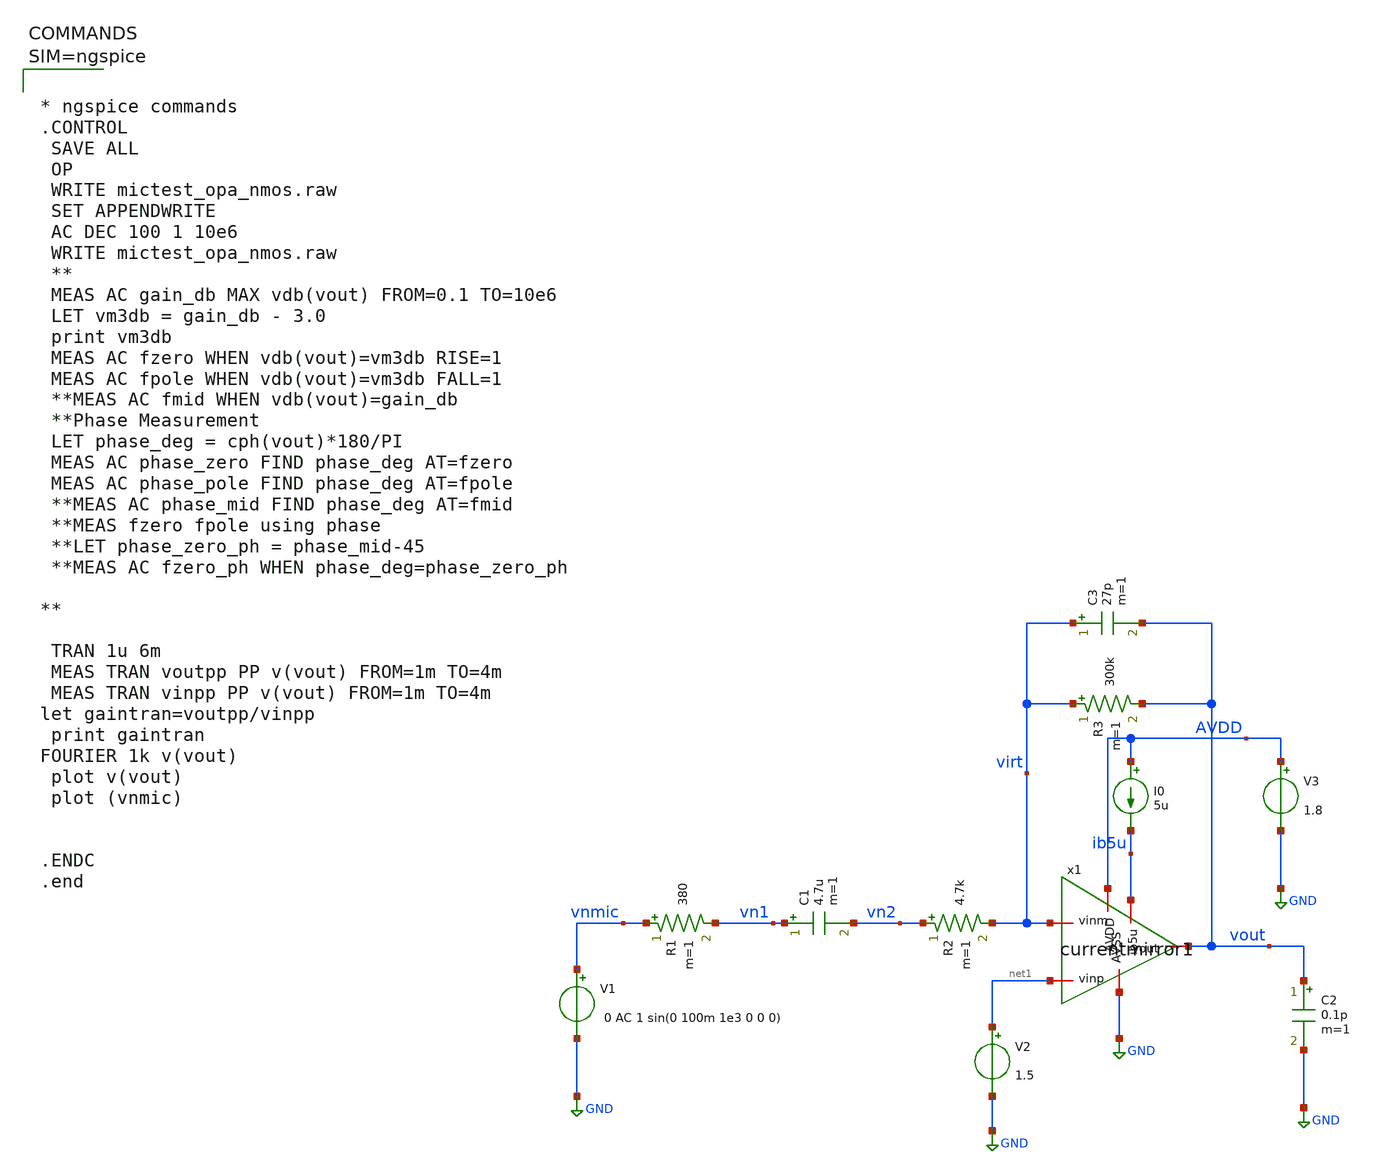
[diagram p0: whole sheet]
** sch_path: xschem/mictest_opamp_nmos.sch
**.subckt mictest_opamp_nmos
x1 AVDD vout virt net1 ib5u GND currentmirror1
R1 vnmic vn1 380 m=1
R2 vn2 virt 4.7k m=1
C1 vn1 vn2 4.7u m=1
V1 vnmic GND 0 AC 1 sin(0 100m 1e3 0 0 0)
I0 AVDD ib5u 5u
V2 net1 GND 1.5
C2 vout GND 0.1p m=1
V3 AVDD GND 1.8
R3 virt vout 300k m=1
C3 virt vout 27p m=1
**** begin user architecture code

** opencircuitdesign pdks install
.lib $::SKYWATER_MODELS/sky130.lib.spice tt




* ngspice commands
.CONTROL
 SAVE ALL
 OP
 WRITE mictest_opa_nmos.raw
 SET APPENDWRITE
 AC DEC 100 1 10e6
 WRITE mictest_opa_nmos.raw
 **
 MEAS AC gain_db MAX vdb(vout) FROM=0.1 TO=10e6
 LET vm3db = gain_db - 3.0
 print vm3db
 MEAS AC fzero WHEN vdb(vout)=vm3db RISE=1
 MEAS AC fpole WHEN vdb(vout)=vm3db FALL=1
 **MEAS AC fmid WHEN vdb(vout)=gain_db
 **Phase Measurement
 LET phase_deg = cph(vout)*180/PI
 MEAS AC phase_zero FIND phase_deg AT=fzero
 MEAS AC phase_pole FIND phase_deg AT=fpole
 **MEAS AC phase_mid FIND phase_deg AT=fmid
 **MEAS fzero fpole using phase
 **LET phase_zero_ph = phase_mid-45
 **MEAS AC fzero_ph WHEN phase_deg=phase_zero_ph

**

 TRAN 1u 6m
 MEAS TRAN voutpp PP v(vout) FROM=1m TO=4m
 MEAS TRAN vinpp PP v(vout) FROM=1m TO=4m
let gaintran=voutpp/vinpp
 print gaintran
FOURIER 1k v(vout)
 plot v(vout)
 plot (vnmic)


.ENDC
.end



**** end user architecture code
**.ends

* expanding   symbol:  currentmirror1.sym # of pins=6
** sym_path: xschem/currentmirror1.sym
** sch_path: xschem/currentmirror1.sch
.subckt currentmirror1 AVDD vout vinm vinp ib5u AVSS
*.iopin vinp
*.iopin vinm
*.iopin AVDD
*.iopin AVSS
*.iopin ib5u
*.iopin vout
XM5 ib5u ib5u AVSS AVSS sky130_fd_pr__nfet_01v8 L=1 W=5 nf=1 ad='int((1 + 1)/2) * 5 / 1 * 0.29' as='int((1 + 2)/2) * 5 / 1 * 0.29'
+ pd='2*int((1 + 1)/2) * (5 / 1 + 0.29)' ps='2*int((1 + 2)/2) * (5 / 1 + 0.29)' nrd='0.29 / 5 ' nrs='0.29 / 5 '
+ sa=0 sb=0 sd=0 mult=1 m=1
XM6 net1 ib5u AVSS AVSS sky130_fd_pr__nfet_01v8 L=1 W=5 nf=1 ad='int((1 + 1)/2) * 5 / 1 * 0.29' as='int((1 + 2)/2) * 5 / 1 * 0.29'
+ pd='2*int((1 + 1)/2) * (5 / 1 + 0.29)' ps='2*int((1 + 2)/2) * (5 / 1 + 0.29)' nrd='0.29 / 5 ' nrs='0.29 / 5 '
+ sa=0 sb=0 sd=0 mult=2 m=2
XM3 net2 vinp net1 net1 sky130_fd_pr__nfet_01v8 L=2 W=5 nf=1 ad='int((1 + 1)/2) * 5 / 1 * 0.29' as='int((1 + 2)/2) * 5 / 1 * 0.29'
+ pd='2*int((1 + 1)/2) * (5 / 1 + 0.29)' ps='2*int((1 + 2)/2) * (5 / 1 + 0.29)' nrd='0.29 / 5 ' nrs='0.29 / 5 '
+ sa=0 sb=0 sd=0 mult=4 m=4
XM4 vout vinm net1 net1 sky130_fd_pr__nfet_01v8 L=2 W=5 nf=1 ad='int((1 + 1)/2) * 5 / 1 * 0.29' as='int((1 + 2)/2) * 5 / 1 * 0.29'
+ pd='2*int((1 + 1)/2) * (5 / 1 + 0.29)' ps='2*int((1 + 2)/2) * (5 / 1 + 0.29)' nrd='0.29 / 5 ' nrs='0.29 / 5 '
+ sa=0 sb=0 sd=0 mult=4 m=4
XM1 net2 net2 AVDD AVDD sky130_fd_pr__pfet_01v8_lvt L=2 W=5 nf=1 ad='int((1 + 1)/2) * 5 / 1 * 0.29' as='int((1 + 2)/2) * 5 / 1 * 0.29'
+ pd='2*int((1 + 1)/2) * (5 / 1 + 0.29)' ps='2*int((1 + 2)/2) * (5 / 1 + 0.29)' nrd='0.29 / 5 ' nrs='0.29 / 5 '
+ sa=0 sb=0 sd=0 mult=2 m=2
XM2 vout net2 AVDD AVDD sky130_fd_pr__pfet_01v8_lvt L=2 W=5 nf=1 ad='int((1 + 1)/2) * 5 / 1 * 0.29' as='int((1 + 2)/2) * 5 / 1 * 0.29'
+ pd='2*int((1 + 1)/2) * (5 / 1 + 0.29)' ps='2*int((1 + 2)/2) * (5 / 1 + 0.29)' nrd='0.29 / 5 ' nrs='0.29 / 5 '
+ sa=0 sb=0 sd=0 mult=2 m=2
.ends

.GLOBAL GND
.end
